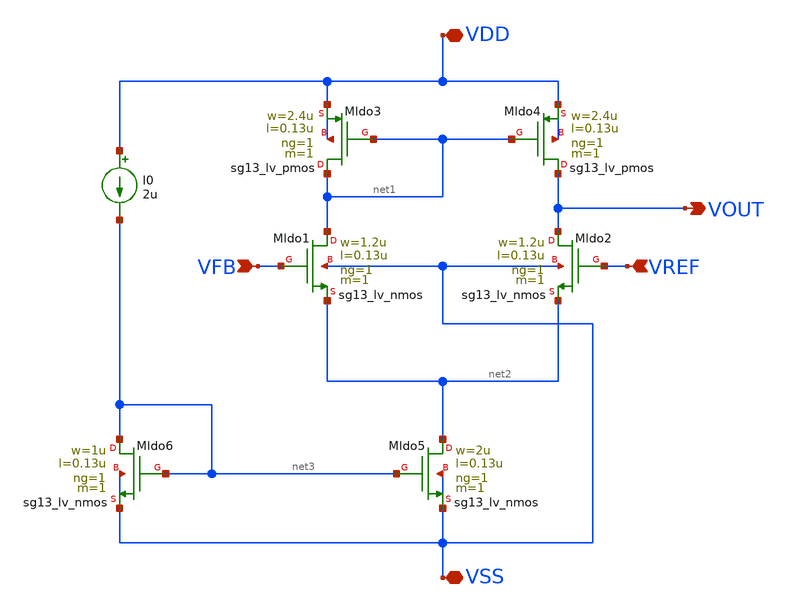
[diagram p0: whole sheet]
** sch_path: analog/core/error_amp.sch
**.subckt error_amp VREF VDD VOUT VFB VSS
*.ipin VREF
*.iopin VDD
*.opin VOUT
*.ipin VFB
*.iopin VSS
XMldo1 net1 VFB net2 VSS sg13_lv_nmos w=1.2u l=0.13u ng=1 m=1 mm_ok=1
XMldo4 VOUT net1 VDD VDD sg13_lv_pmos w=2.4u l=0.13u ng=1 m=1 mm_ok=1
XMldo2 VOUT VREF net2 VSS sg13_lv_nmos w=1.2u l=0.13u ng=1 m=1 mm_ok=1
XMldo3 net1 net1 VDD VDD sg13_lv_pmos w=2.4u l=0.13u ng=1 m=1 mm_ok=1
XMldo5 net2 net3 VSS VSS sg13_lv_nmos w=2u l=0.13u ng=1 m=1 mm_ok=1
XMldo6 net3 net3 VSS VSS sg13_lv_nmos w=1u l=0.13u ng=1 m=1 mm_ok=1
I0 VDD net3 2u
**.ends
.end
